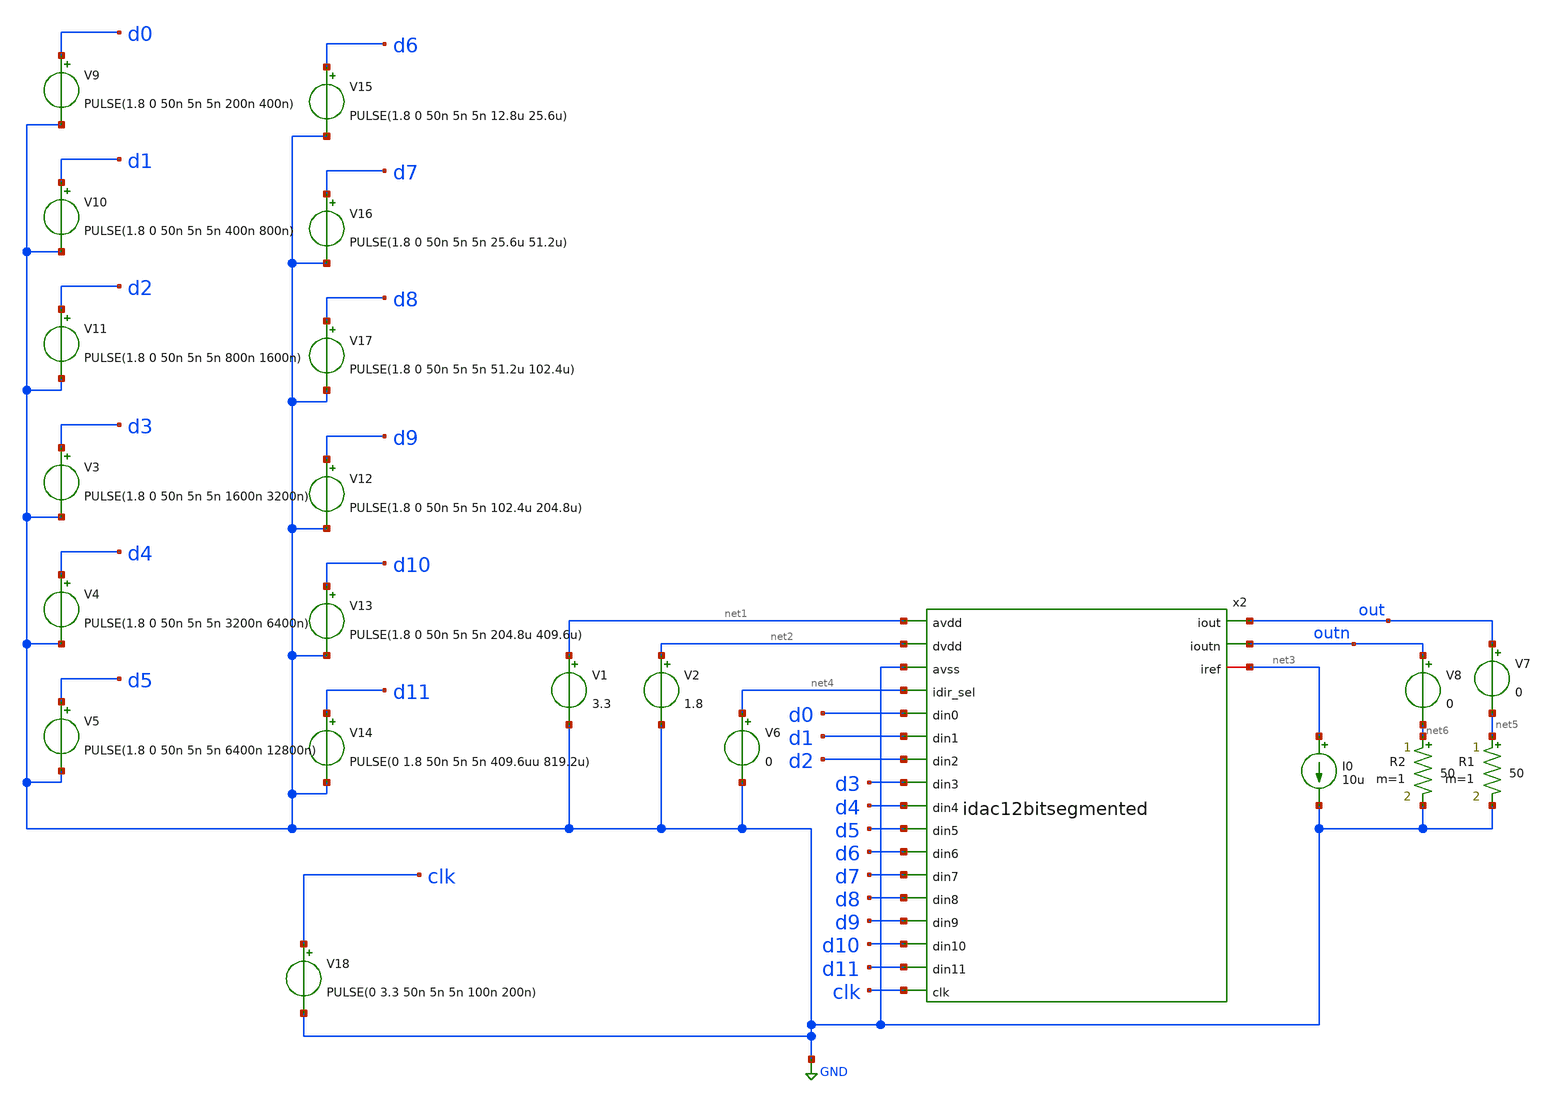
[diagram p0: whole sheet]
** sch_path: xschem/idac12bitsegmented_cs_tb.sch
**.subckt idac12bitsegmented_cs_tb
V1 net1 GND 3.3
V2 net2 GND 1.8
I0 net3 GND 10u
V3 d3 GND PULSE(1.8 0 50n 5n 5n 1600n 3200n)
V4 d4 GND PULSE(1.8 0 50n 5n 5n 3200n 6400n)
V5 d5 GND PULSE(1.8 0 50n 5n 5n 6400n 12800n)
V6 net4 GND 0
V7 out net5 0
R1 net5 GND 50 m=1
V8 outn net6 0
R2 net6 GND 50 m=1
V9 d0 GND PULSE(1.8 0 50n 5n 5n 200n 400n)
V10 d1 GND PULSE(1.8 0 50n 5n 5n 400n 800n)
V11 d2 GND PULSE(1.8 0 50n 5n 5n 800n 1600n)
x2 out net1 net2 outn GND net3 net4 d0 d1 d2 d3 d4 d5 d6 d7 d8 d9 d10 d11 clk idac12bitsegmented
V12 d9 GND PULSE(1.8 0 50n 5n 5n 102.4u 204.8u)
V13 d10 GND PULSE(1.8 0 50n 5n 5n 204.8u 409.6u)
V14 d11 GND PULSE(0 1.8 50n 5n 5n 409.6uu 819.2u)
V15 d6 GND PULSE(1.8 0 50n 5n 5n 12.8u 25.6u)
V16 d7 GND PULSE(1.8 0 50n 5n 5n 25.6u 51.2u)
V17 d8 GND PULSE(1.8 0 50n 5n 5n 51.2u 102.4u)
V18 clk GND PULSE(0 3.3 50n 5n 5n 100n 200n)
**** begin user architecture code
 .lib $::SKYWATER_MODELS/sky130.lib.spice tt
.include $::SKYWATER_STDCELLS/../../sky130_fd_sc_hvl/spice/sky130_fd_sc_hvl.spice

.param mc_mm_switch=0
.param mc_pr_switch=1



.option wnflag=0
.save v(out) i(V7)
.control
tran 500n 3.2u
plot v(out)
plot i(V7)
write idac2.raw v(out)
.endc


**** end user architecture code
**.ends
.GLOBAL GND
.end
